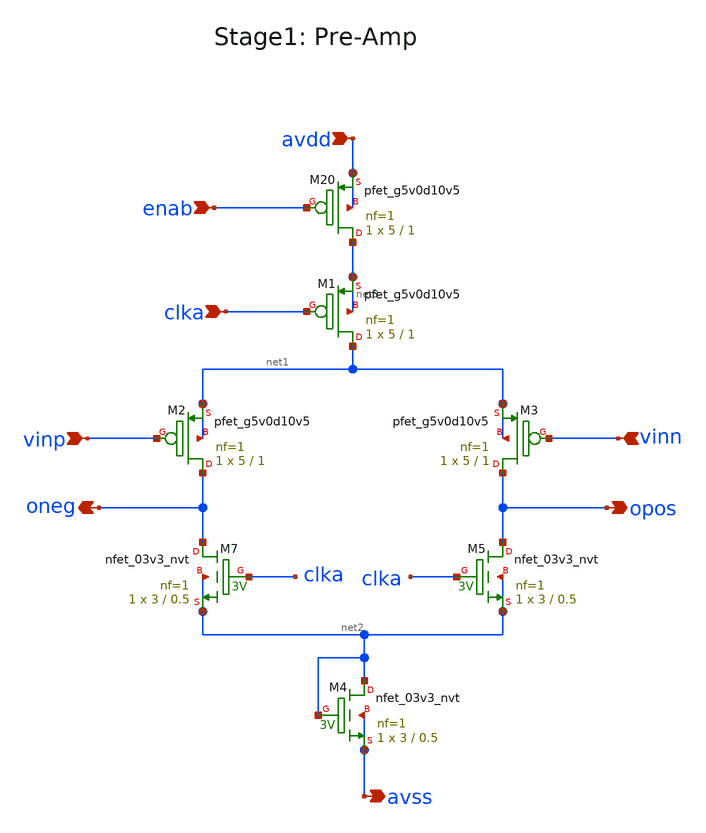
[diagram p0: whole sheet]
** sch_path: xschem/Stage1.sch
**.subckt Stage1 avdd vinp vinn avss clka opos oneg enab
*.ipin avdd
*.ipin vinp
*.ipin vinn
*.opin avss
*.ipin clka
*.opin opos
*.opin oneg
*.ipin enab
XM2 oneg vinp net1 net1 sky130_fd_pr__pfet_g5v0d10v5 L=1 W=5 nf=1 ad='int((nf+1)/2) * W/nf * 0.29' as='int((nf+2)/2) * W/nf * 0.29'
+ pd='2*int((nf+1)/2) * (W/nf + 0.29)' ps='2*int((nf+2)/2) * (W/nf + 0.29)' nrd='0.29 / W' nrs='0.29 / W'
+ sa=0 sb=0 sd=0 mult=1 m=1
XM3 opos vinn net1 net1 sky130_fd_pr__pfet_g5v0d10v5 L=1 W=5 nf=1 ad='int((nf+1)/2) * W/nf * 0.29' as='int((nf+2)/2) * W/nf * 0.29'
+ pd='2*int((nf+1)/2) * (W/nf + 0.29)' ps='2*int((nf+2)/2) * (W/nf + 0.29)' nrd='0.29 / W' nrs='0.29 / W'
+ sa=0 sb=0 sd=0 mult=1 m=1
XM7 oneg clka net2 net2 sky130_fd_pr__nfet_03v3_nvt L=0.5 W=3 nf=1 ad='int((nf+1)/2) * W/nf * 0.29' as='int((nf+2)/2) * W/nf * 0.29'
+ pd='2*int((nf+1)/2) * (W/nf + 0.29)' ps='2*int((nf+2)/2) * (W/nf + 0.29)' nrd='0.29 / W' nrs='0.29 / W'
+ sa=0 sb=0 sd=0 mult=1 m=1
XM5 opos clka net2 net2 sky130_fd_pr__nfet_03v3_nvt L=0.5 W=3 nf=1 ad='int((nf+1)/2) * W/nf * 0.29' as='int((nf+2)/2) * W/nf * 0.29'
+ pd='2*int((nf+1)/2) * (W/nf + 0.29)' ps='2*int((nf+2)/2) * (W/nf + 0.29)' nrd='0.29 / W' nrs='0.29 / W'
+ sa=0 sb=0 sd=0 mult=1 m=1
XM4 net2 net2 avss avss sky130_fd_pr__nfet_03v3_nvt L=0.5 W=3 nf=1 ad='int((nf+1)/2) * W/nf * 0.29' as='int((nf+2)/2) * W/nf * 0.29'
+ pd='2*int((nf+1)/2) * (W/nf + 0.29)' ps='2*int((nf+2)/2) * (W/nf + 0.29)' nrd='0.29 / W' nrs='0.29 / W'
+ sa=0 sb=0 sd=0 mult=1 m=1
XM20 net3 enab avdd avdd sky130_fd_pr__pfet_g5v0d10v5 L=1 W=5 nf=1 ad='int((nf+1)/2) * W/nf * 0.29' as='int((nf+2)/2) * W/nf * 0.29'
+ pd='2*int((nf+1)/2) * (W/nf + 0.29)' ps='2*int((nf+2)/2) * (W/nf + 0.29)' nrd='0.29 / W' nrs='0.29 / W'
+ sa=0 sb=0 sd=0 mult=1 m=1
XM1 net1 clka net3 net3 sky130_fd_pr__pfet_g5v0d10v5 L=1 W=5 nf=1 ad='int((nf+1)/2) * W/nf * 0.29' as='int((nf+2)/2) * W/nf * 0.29'
+ pd='2*int((nf+1)/2) * (W/nf + 0.29)' ps='2*int((nf+2)/2) * (W/nf + 0.29)' nrd='0.29 / W' nrs='0.29 / W'
+ sa=0 sb=0 sd=0 mult=1 m=1
**.ends
.end
